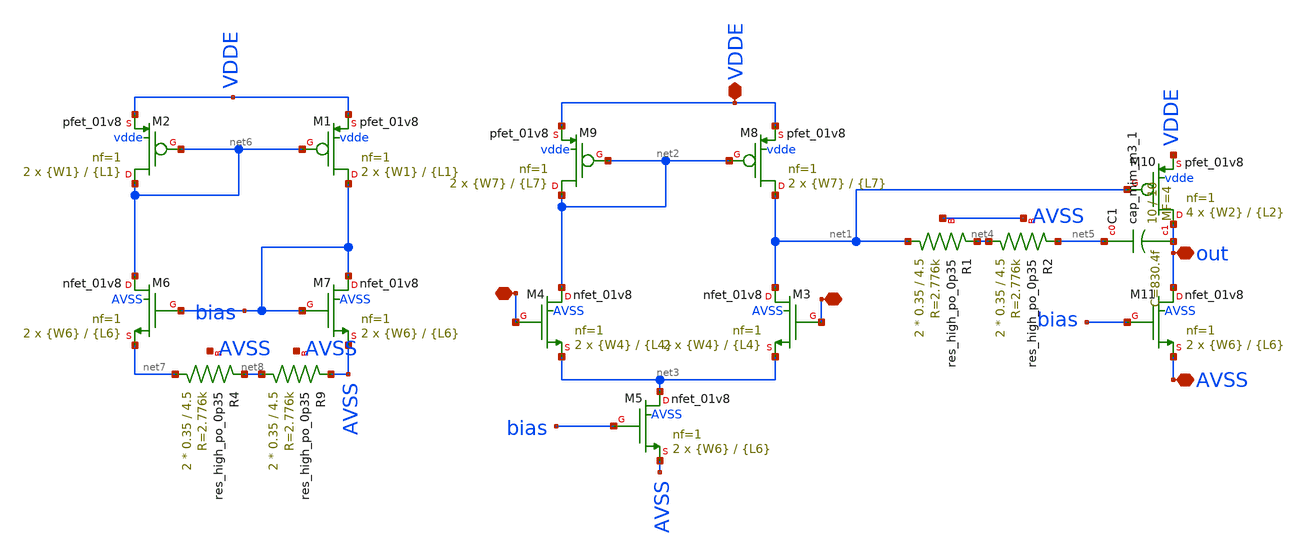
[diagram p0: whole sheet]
** sch_path: xschem/op5.sch
**.subckt op5 AVSS - + VDDE out
*.iopin AVSS
*.iopin -
*.iopin +
*.iopin VDDE
*.iopin out
XM8 net1 net2 VDDE vdde sky130_fd_pr__pfet_01v8 L={L7} W={W7} nf=1 ad='int((nf+1)/2) * W/nf * 0.29' as='int((nf+2)/2) * W/nf * 0.29'
+ pd='2*int((nf+1)/2) * (W/nf + 0.29)' ps='2*int((nf+2)/2) * (W/nf + 0.29)' nrd='0.29 / W' nrs='0.29 / W'
+ sa=0 sb=0 sd=0 mult=2 m=2
XM9 net2 net2 VDDE vdde sky130_fd_pr__pfet_01v8 L={L7} W={W7} nf=1 ad='int((nf+1)/2) * W/nf * 0.29' as='int((nf+2)/2) * W/nf * 0.29'
+ pd='2*int((nf+1)/2) * (W/nf + 0.29)' ps='2*int((nf+2)/2) * (W/nf + 0.29)' nrd='0.29 / W' nrs='0.29 / W'
+ sa=0 sb=0 sd=0 mult=2 m=2
XM5 net3 bias AVSS AVSS sky130_fd_pr__nfet_01v8 L={L6} W={W6} nf=1 ad='int((nf+1)/2) * W/nf * 0.29' as='int((nf+2)/2) * W/nf * 0.29'
+ pd='2*int((nf+1)/2) * (W/nf + 0.29)' ps='2*int((nf+2)/2) * (W/nf + 0.29)' nrd='0.29 / W' nrs='0.29 / W'
+ sa=0 sb=0 sd=0 mult=2 m=2
XM10 out net1 VDDE vdde sky130_fd_pr__pfet_01v8 L={L2} W={W2} nf=1 ad='int((nf+1)/2) * W/nf * 0.29' as='int((nf+2)/2) * W/nf * 0.29'
+ pd='2*int((nf+1)/2) * (W/nf + 0.29)' ps='2*int((nf+2)/2) * (W/nf + 0.29)' nrd='0.29 / W' nrs='0.29 / W'
+ sa=0 sb=0 sd=0 mult=4 m=4
XM11 out bias AVSS AVSS sky130_fd_pr__nfet_01v8 L={L6} W={W6} nf=1 ad='int((nf+1)/2) * W/nf * 0.29' as='int((nf+2)/2) * W/nf * 0.29'
+ pd='2*int((nf+1)/2) * (W/nf + 0.29)' ps='2*int((nf+2)/2) * (W/nf + 0.29)' nrd='0.29 / W' nrs='0.29 / W'
+ sa=0 sb=0 sd=0 mult=2 m=2
XM3 net1 + net3 AVSS sky130_fd_pr__nfet_01v8 L={L4} W={W4} nf=1 ad='int((nf+1)/2) * W/nf * 0.29' as='int((nf+2)/2) * W/nf * 0.29'
+ pd='2*int((nf+1)/2) * (W/nf + 0.29)' ps='2*int((nf+2)/2) * (W/nf + 0.29)' nrd='0.29 / W' nrs='0.29 / W'
+ sa=0 sb=0 sd=0 mult=2 m=2
XM1 bias net6 VDDE vdde sky130_fd_pr__pfet_01v8 L={L1} W={W1} nf=1 ad='int((nf+1)/2) * W/nf * 0.29' as='int((nf+2)/2) * W/nf * 0.29'
+ pd='2*int((nf+1)/2) * (W/nf + 0.29)' ps='2*int((nf+2)/2) * (W/nf + 0.29)' nrd='0.29 / W' nrs='0.29 / W'
+ sa=0 sb=0 sd=0 mult=2 m=2
XM2 net6 net6 VDDE vdde sky130_fd_pr__pfet_01v8 L={L1} W={W1} nf=1 ad='int((nf+1)/2) * W/nf * 0.29' as='int((nf+2)/2) * W/nf * 0.29'
+ pd='2*int((nf+1)/2) * (W/nf + 0.29)' ps='2*int((nf+2)/2) * (W/nf + 0.29)' nrd='0.29 / W' nrs='0.29 / W'
+ sa=0 sb=0 sd=0 mult=2 m=2
XM6 net6 bias net7 AVSS sky130_fd_pr__nfet_01v8 L={L6} W={W6} nf=1 ad='int((nf+1)/2) * W/nf * 0.29' as='int((nf+2)/2) * W/nf * 0.29'
+ pd='2*int((nf+1)/2) * (W/nf + 0.29)' ps='2*int((nf+2)/2) * (W/nf + 0.29)' nrd='0.29 / W' nrs='0.29 / W'
+ sa=0 sb=0 sd=0 mult=2 m=2
XM7 bias bias AVSS AVSS sky130_fd_pr__nfet_01v8 L={L6} W={W6} nf=1 ad='int((nf+1)/2) * W/nf * 0.29' as='int((nf+2)/2) * W/nf * 0.29'
+ pd='2*int((nf+1)/2) * (W/nf + 0.29)' ps='2*int((nf+2)/2) * (W/nf + 0.29)' nrd='0.29 / W' nrs='0.29 / W'
+ sa=0 sb=0 sd=0 mult=2 m=2
XR4 net7 net8 AVSS sky130_fd_pr__res_high_po_0p35 L=4.5 mult=2 m=2
XM4 net2 - net3 AVSS sky130_fd_pr__nfet_01v8 L={L4} W={W4} nf=1 ad='int((nf+1)/2) * W/nf * 0.29' as='int((nf+2)/2) * W/nf * 0.29'
+ pd='2*int((nf+1)/2) * (W/nf + 0.29)' ps='2*int((nf+2)/2) * (W/nf + 0.29)' nrd='0.29 / W' nrs='0.29 / W'
+ sa=0 sb=0 sd=0 mult=2 m=2
XR1 net1 net4 AVSS sky130_fd_pr__res_high_po_0p35 L=4.5 mult=2 m=2
XR2 net4 net5 AVSS sky130_fd_pr__res_high_po_0p35 L=4.5 mult=2 m=2
XR9 net8 AVSS AVSS sky130_fd_pr__res_high_po_0p35 L=4.5 mult=2 m=2
XC1 net5 out sky130_fd_pr__cap_mim_m3_1 W=10 L=10 MF=4 m=4
**** begin user architecture code


.include /home/gils/sky130_pdk/share/pdk/sky130A/libs.ref/sky130_fd_pr/spice/sky130_fd_pr__cap_vpp_11p5x11p7_l1m1m2m3_shieldm4.model.spice
**************
*PMOS cms
.param L1=10
.param W1=1

**************
*PMOS current differential
.param L7=10
.param W7=1

**************
*differential Pair
.param L4=13
.param W4=0.9

**************
*NMOS current control
.param L6=20
.param W6=1

**************
*Second Stage
.param L2=10
.param W2=1


**** end user architecture code
**.ends
.end
